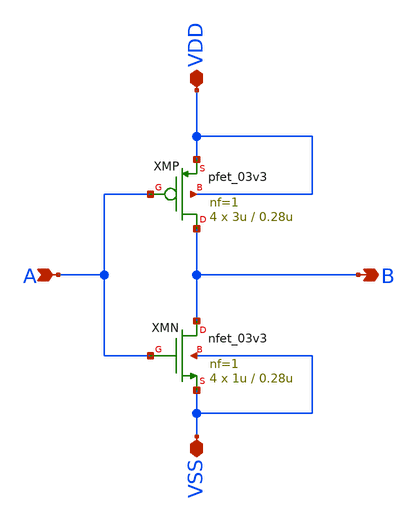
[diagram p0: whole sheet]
** sch_path: designs/DS_modulator/gate_inv_L0d28_x4/xschem/gate_inv_L0d28_x4.sch
**.subckt gate_inv_L0d28_x4 B A VDD VSS
*.opin B
*.ipin A
*.iopin VDD
*.iopin VSS
XMN B A VSS VSS nfet_03v3 L=0.28u W=1u nf=1 ad='int((nf+1)/2) * W/nf * 0.18u' as='int((nf+2)/2) * W/nf * 0.18u'
+ pd='2*int((nf+1)/2) * (W/nf + 0.18u)' ps='2*int((nf+2)/2) * (W/nf + 0.18u)' nrd='0.18u / W' nrs='0.18u / W'
+ sa=0 sb=0 sd=0 m=4
XMP B A VDD VDD pfet_03v3 L=0.28u W=3u nf=1 ad='int((nf+1)/2) * W/nf * 0.18u' as='int((nf+2)/2) * W/nf * 0.18u'
+ pd='2*int((nf+1)/2) * (W/nf + 0.18u)' ps='2*int((nf+2)/2) * (W/nf + 0.18u)' nrd='0.18u / W' nrs='0.18u / W'
+ sa=0 sb=0 sd=0 m=4
**.ends
.end
